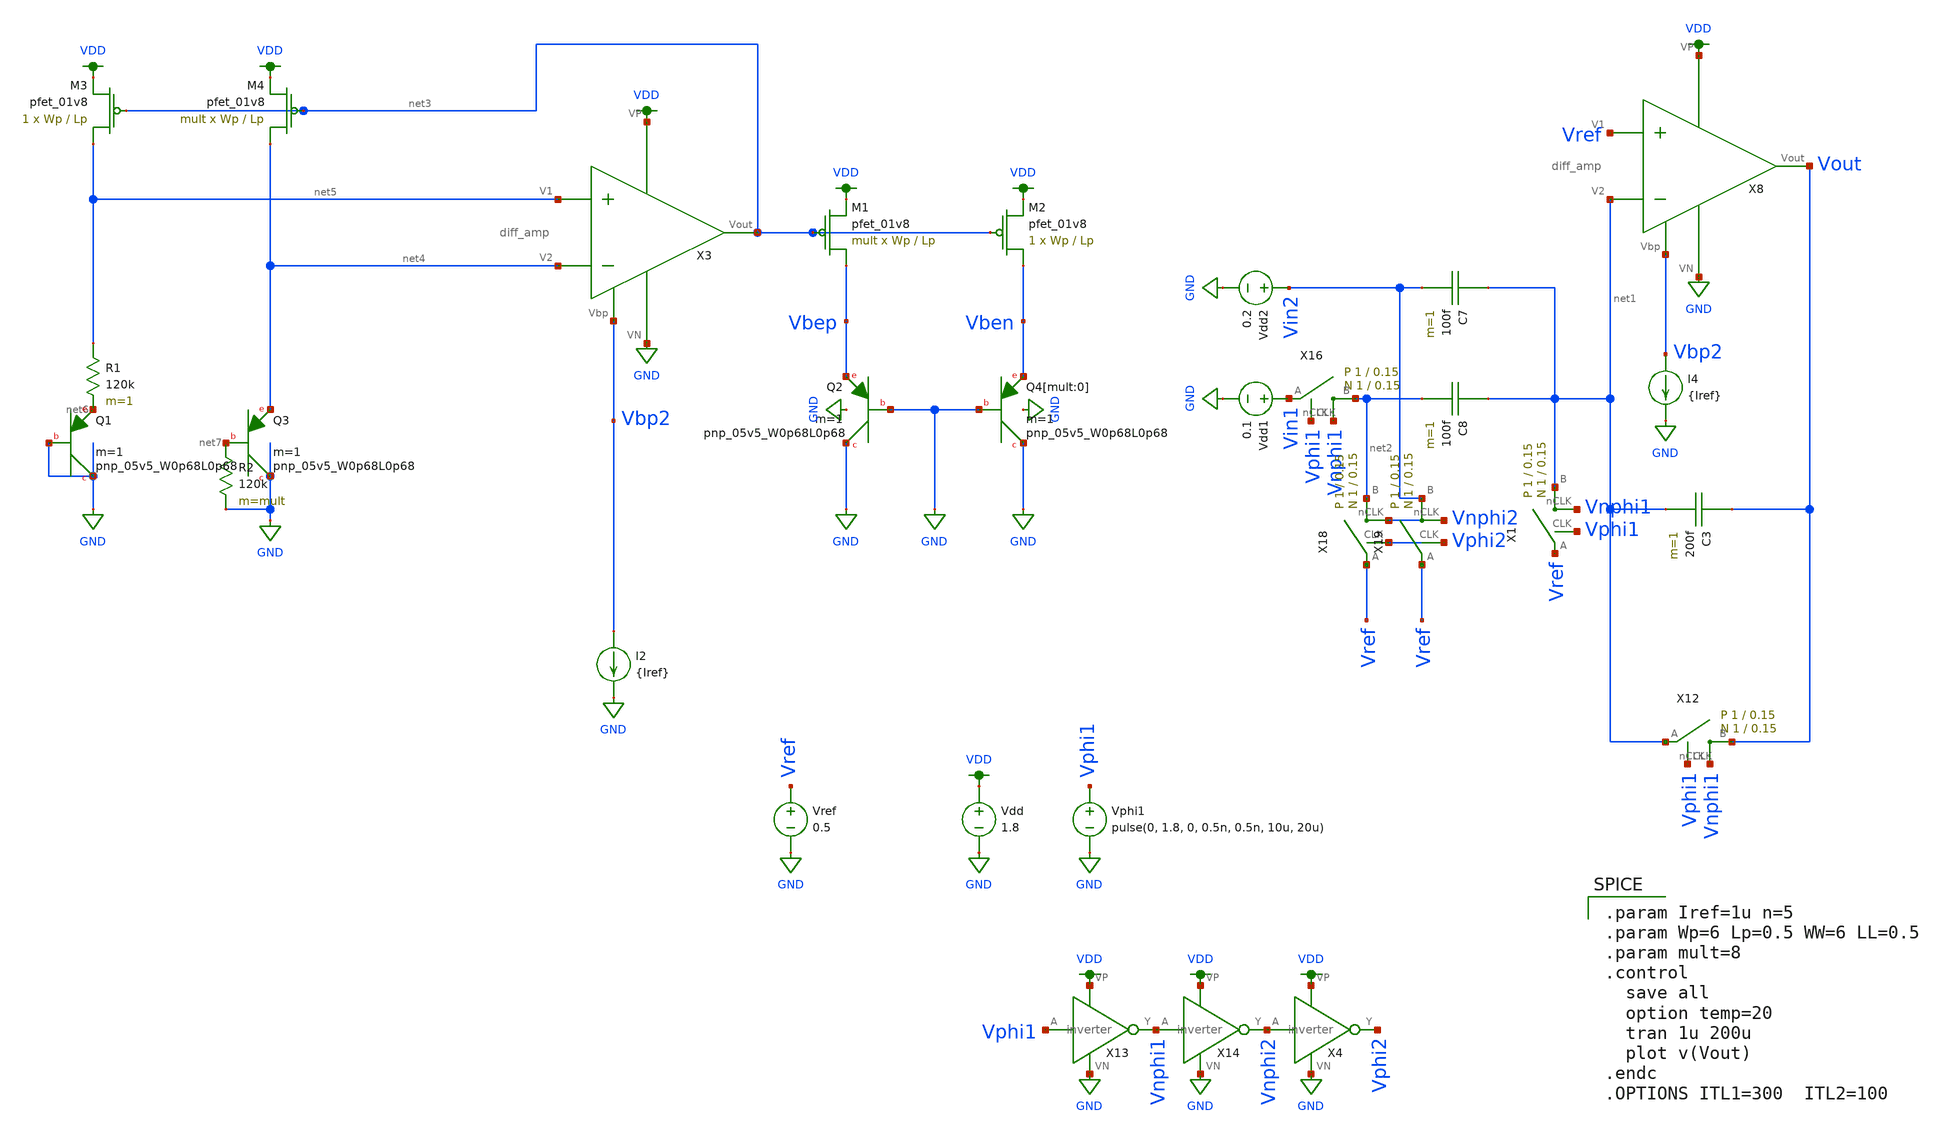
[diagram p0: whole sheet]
** sch_path: schematic/test/vadd_test.sch
**.subckt vadd_test
X8 VDD Vbp2 Vout Vref net1 GND diff_amp
I4 Vbp2 GND {Iref}
C3 Vout net1 200f m=1
C7 net1 Vin2 100f m=1
C8 net1 net2 100f m=1
X16 net2 Vin1 Vphi1 Vnphi1 switch Wp=1 Lp=0.15 WW=1 LL=0.15
X18 net2 Vref Vphi2 Vnphi2 switch Wp=1 Lp=0.15 WW=1 LL=0.15
X19 Vin2 Vref Vphi2 Vnphi2 switch Wp=1 Lp=0.15 WW=1 LL=0.15
Vphi1 Vphi1 GND pulse(0, 1.8, 0, 0.5n, 0.5n, 10u, 20u)
X13 Vphi1 Vnphi1 VDD GND inverter
X14 Vnphi1 Vnphi2 VDD GND inverter
X4 Vnphi2 Vphi2 VDD GND inverter
Vdd VDD GND 1.8
Vref Vref GND 0.5
X12 Vout net1 Vphi1 Vnphi1 switch Wp=1 Lp=0.15 WW=1 LL=0.15
X1 net1 Vref Vphi1 Vnphi1 switch Wp=1 Lp=0.15 WW=1 LL=0.15
XQ2 GND GND Vbep sky130_fd_pr__pnp_05v5_W0p68L0p68 m=1
XM1 Vbep net3 VDD VDD sky130_fd_pr__pfet_01v8 L=Lp W=Wp nf=1 ad='int((nf+1)/2) * W/nf * 0.29' as='int((nf+2)/2) * W/nf * 0.29'
+ pd='2*int((nf+1)/2) * (W/nf + 0.29)' ps='2*int((nf+2)/2) * (W/nf + 0.29)' nrd='0.29 / W' nrs='0.29 / W'
+ sa=0 sb=0 sd=0 mult=mult m=mult
XM2 Vben net3 VDD VDD sky130_fd_pr__pfet_01v8 L=Lp W=Wp nf=1 ad='int((nf+1)/2) * W/nf * 0.29' as='int((nf+2)/2) * W/nf * 0.29'
+ pd='2*int((nf+1)/2) * (W/nf + 0.29)' ps='2*int((nf+2)/2) * (W/nf + 0.29)' nrd='0.29 / W' nrs='0.29 / W'
+ sa=0 sb=0 sd=0 mult=1 m=1
XQ4[mult:0] GND GND Vben sky130_fd_pr__pnp_05v5_W0p68L0p68 m=1
XQ1 GND GND net6 sky130_fd_pr__pnp_05v5_W0p68L0p68 m=1
XQ3 GND net7 net4 sky130_fd_pr__pnp_05v5_W0p68L0p68 m=1
R1 net5 net6 120k m=1
R2 net7 GND 120k m=mult
XM3 net5 net3 VDD VDD sky130_fd_pr__pfet_01v8 L=Lp W=Wp nf=1 ad='int((nf+1)/2) * W/nf * 0.29' as='int((nf+2)/2) * W/nf * 0.29'
+ pd='2*int((nf+1)/2) * (W/nf + 0.29)' ps='2*int((nf+2)/2) * (W/nf + 0.29)' nrd='0.29 / W' nrs='0.29 / W'
+ sa=0 sb=0 sd=0 mult=1 m=1
XM4 net4 net3 VDD VDD sky130_fd_pr__pfet_01v8 L=Lp W=Wp nf=1 ad='int((nf+1)/2) * W/nf * 0.29' as='int((nf+2)/2) * W/nf * 0.29'
+ pd='2*int((nf+1)/2) * (W/nf + 0.29)' ps='2*int((nf+2)/2) * (W/nf + 0.29)' nrd='0.29 / W' nrs='0.29 / W'
+ sa=0 sb=0 sd=0 mult=mult m=mult
X3 VDD Vbp2 net3 net5 net4 GND diff_amp
I2 Vbp2 GND {Iref}
Vdd1 Vin1 GND 0.1
Vdd2 Vin2 GND 0.2
**** begin user architecture code

.param Iref=1u n=5
.param Wp=6 Lp=0.5 WW=6 LL=0.5
.param mult=8
.control
  save all
  option temp=20
  tran 1u 200u
  plot v(Vout)
.endc
.OPTIONS ITL1=300  ITL2=100


.option wnflag=1
.param MC_SWITCH=0.0
.lib /media/qdeng/526448C32060CF5C/skywater/skywater-pdk/libraries/sky130_fd_pr_ngspice/latest/models/sky130.lib.spice tt

**** end user architecture code
**.ends
.GLOBAL GND
.GLOBAL VDD
.end
